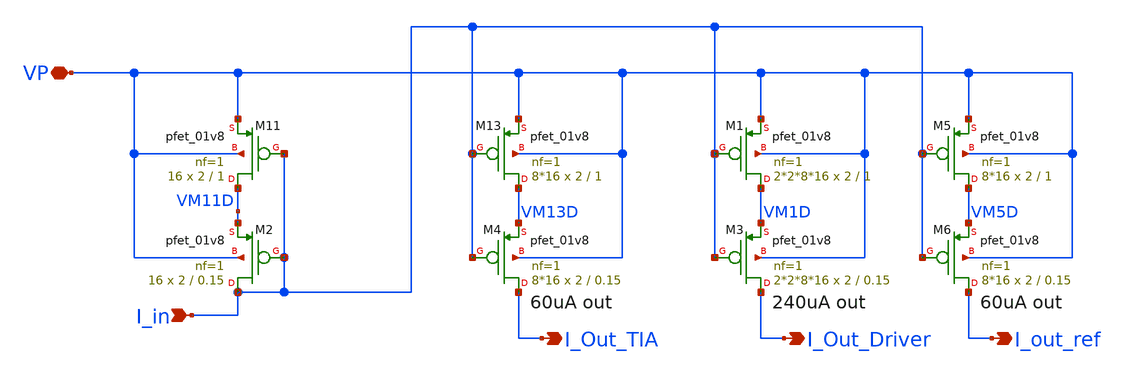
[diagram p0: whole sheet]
** sch_path: xschem/bias/current_mirror_channel.sch
**.subckt current_mirror_channel I_in VP I_Out_TIA I_Out_Driver I_out_ref
*.ipin I_in
*.iopin VP
*.opin I_Out_TIA
*.opin I_Out_Driver
*.opin I_out_ref
XM13 VM13D I_in VP VP sky130_fd_pr__pfet_01v8 L=1 W=2 nf=1 ad='int((nf+1)/2) * W/nf * 0.29' as='int((nf+2)/2) * W/nf * 0.29'
+ pd='2*int((nf+1)/2) * (W/nf + 0.29)' ps='2*int((nf+2)/2) * (W/nf + 0.29)' nrd='0.29 / W' nrs='0.29 / W'
+ sa=0 sb=0 sd=0 mult=8*16 m=8*16
XM11 VM11D I_in VP VP sky130_fd_pr__pfet_01v8 L=1 W=2 nf=1 ad='int((nf+1)/2) * W/nf * 0.29' as='int((nf+2)/2) * W/nf * 0.29'
+ pd='2*int((nf+1)/2) * (W/nf + 0.29)' ps='2*int((nf+2)/2) * (W/nf + 0.29)' nrd='0.29 / W' nrs='0.29 / W'
+ sa=0 sb=0 sd=0 mult=16 m=16
XM2 I_in I_in VM11D VP sky130_fd_pr__pfet_01v8 L=0.15 W=2 nf=1 ad='int((nf+1)/2) * W/nf * 0.29' as='int((nf+2)/2) * W/nf * 0.29'
+ pd='2*int((nf+1)/2) * (W/nf + 0.29)' ps='2*int((nf+2)/2) * (W/nf + 0.29)' nrd='0.29 / W' nrs='0.29 / W'
+ sa=0 sb=0 sd=0 mult=16 m=16
XM4 I_Out_TIA I_in VM13D VP sky130_fd_pr__pfet_01v8 L=0.15 W=2 nf=1 ad='int((nf+1)/2) * W/nf * 0.29'
+ as='int((nf+2)/2) * W/nf * 0.29' pd='2*int((nf+1)/2) * (W/nf + 0.29)' ps='2*int((nf+2)/2) * (W/nf + 0.29)'
+ nrd='0.29 / W' nrs='0.29 / W' sa=0 sb=0 sd=0 mult=8*16 m=8*16
XM1 VM1D I_in VP VP sky130_fd_pr__pfet_01v8 L=1 W=2 nf=1 ad='int((nf+1)/2) * W/nf * 0.29' as='int((nf+2)/2) * W/nf * 0.29'
+ pd='2*int((nf+1)/2) * (W/nf + 0.29)' ps='2*int((nf+2)/2) * (W/nf + 0.29)' nrd='0.29 / W' nrs='0.29 / W'
+ sa=0 sb=0 sd=0 mult=2*2*8*16 m=2*2*8*16
XM3 I_Out_Driver I_in VM1D VP sky130_fd_pr__pfet_01v8 L=0.15 W=2 nf=1 ad='int((nf+1)/2) * W/nf * 0.29'
+ as='int((nf+2)/2) * W/nf * 0.29' pd='2*int((nf+1)/2) * (W/nf + 0.29)' ps='2*int((nf+2)/2) * (W/nf + 0.29)'
+ nrd='0.29 / W' nrs='0.29 / W' sa=0 sb=0 sd=0 mult=2*2*8*16 m=2*2*8*16
XM5 VM5D I_in VP VP sky130_fd_pr__pfet_01v8 L=1 W=2 nf=1 ad='int((nf+1)/2) * W/nf * 0.29' as='int((nf+2)/2) * W/nf * 0.29'
+ pd='2*int((nf+1)/2) * (W/nf + 0.29)' ps='2*int((nf+2)/2) * (W/nf + 0.29)' nrd='0.29 / W' nrs='0.29 / W'
+ sa=0 sb=0 sd=0 mult=8*16 m=8*16
XM6 I_out_ref I_in VM5D VP sky130_fd_pr__pfet_01v8 L=0.15 W=2 nf=1 ad='int((nf+1)/2) * W/nf * 0.29' as='int((nf+2)/2) * W/nf * 0.29'
+ pd='2*int((nf+1)/2) * (W/nf + 0.29)' ps='2*int((nf+2)/2) * (W/nf + 0.29)' nrd='0.29 / W' nrs='0.29 / W'
+ sa=0 sb=0 sd=0 mult=8*16 m=8*16
**.ends
.end
